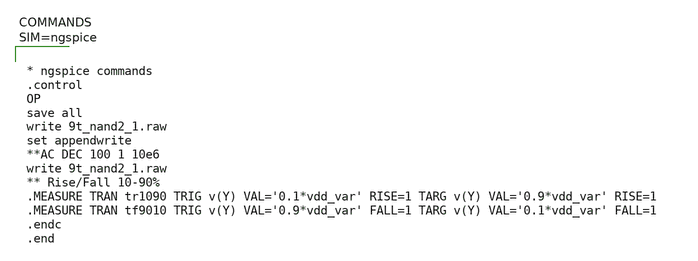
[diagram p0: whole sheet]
** sch_path: xschem/untitled.sch
**.subckt untitled
**** begin user architecture code



* ngspice commands
.control
OP
save all
write 9t_nand2_1.raw
set appendwrite
**AC DEC 100 1 10e6
write 9t_nand2_1.raw
** Rise/Fall 10-90%
.MEASURE TRAN tr1090 TRIG v(Y) VAL='0.1*vdd_var' RISE=1 TARG v(Y) VAL='0.9*vdd_var' RISE=1
.MEASURE TRAN tf9010 TRIG v(Y) VAL='0.9*vdd_var' FALL=1 TARG v(Y) VAL='0.1*vdd_var' FALL=1
.endc
.end



**** end user architecture code
**.ends
.end
